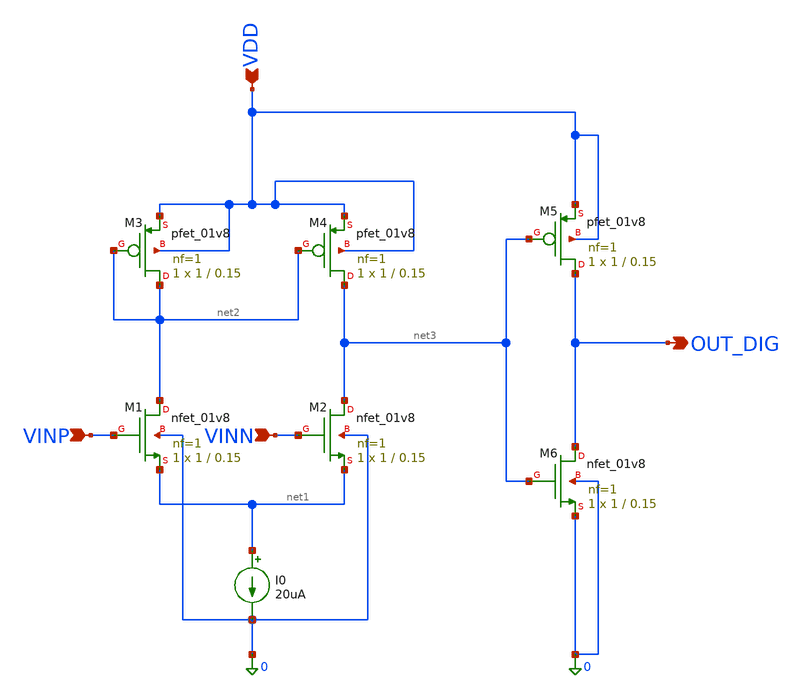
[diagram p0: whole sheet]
** sch_path: comparator.sch
**.subckt comparator VINP VINN VDD OUT_DIG
*.ipin VINP
*.ipin VINN
*.ipin VDD
*.opin OUT_DIG
I0 net1 0 20uA
XM1 net2 VINP net1 0 sky130_fd_pr__nfet_01v8 L=0.15 W=1 nf=1 ad='int((1 + 1)/2) * 1 / 1 * 0.29' as='int((1 + 2)/2) * 1 / 1 * 0.29'
+ pd='2*int((1 + 1)/2) * (1 / 1 + 0.29)' ps='2*int((1 + 2)/2) * (1 / 1 + 0.29)' nrd='0.29 / 1 ' nrs='0.29 / 1 '
+ sa=0 sb=0 sd=0 mult=1 m=1
XM2 net3 VINN net1 0 sky130_fd_pr__nfet_01v8 L=0.15 W=1 nf=1 ad='int((1 + 1)/2) * 1 / 1 * 0.29' as='int((1 + 2)/2) * 1 / 1 * 0.29'
+ pd='2*int((1 + 1)/2) * (1 / 1 + 0.29)' ps='2*int((1 + 2)/2) * (1 / 1 + 0.29)' nrd='0.29 / 1 ' nrs='0.29 / 1 '
+ sa=0 sb=0 sd=0 mult=1 m=1
XM6 OUT_DIG net3 0 0 sky130_fd_pr__nfet_01v8 L=0.15 W=1 nf=1 ad='int((1 + 1)/2) * 1 / 1 * 0.29' as='int((1 + 2)/2) * 1 / 1 * 0.29'
+ pd='2*int((1 + 1)/2) * (1 / 1 + 0.29)' ps='2*int((1 + 2)/2) * (1 / 1 + 0.29)' nrd='0.29 / 1 ' nrs='0.29 / 1 '
+ sa=0 sb=0 sd=0 mult=1 m=1
XM3 net2 net2 VDD VDD sky130_fd_pr__pfet_01v8 L=0.15 W=1 nf=1 ad='int((1 + 1)/2) * 1 / 1 * 0.29' as='int((1 + 2)/2) * 1 / 1 * 0.29'
+ pd='2*int((1 + 1)/2) * (1 / 1 + 0.29)' ps='2*int((1 + 2)/2) * (1 / 1 + 0.29)' nrd='0.29 / 1 ' nrs='0.29 / 1 '
+ sa=0 sb=0 sd=0 mult=1 m=1
XM4 net3 net2 VDD VDD sky130_fd_pr__pfet_01v8 L=0.15 W=1 nf=1 ad='int((1 + 1)/2) * 1 / 1 * 0.29' as='int((1 + 2)/2) * 1 / 1 * 0.29'
+ pd='2*int((1 + 1)/2) * (1 / 1 + 0.29)' ps='2*int((1 + 2)/2) * (1 / 1 + 0.29)' nrd='0.29 / 1 ' nrs='0.29 / 1 '
+ sa=0 sb=0 sd=0 mult=1 m=1
XM5 OUT_DIG net3 VDD VDD sky130_fd_pr__pfet_01v8 L=0.15 W=1 nf=1 ad='int((1 + 1)/2) * 1 / 1 * 0.29' as='int((1 + 2)/2) * 1 / 1 * 0.29'
+ pd='2*int((1 + 1)/2) * (1 / 1 + 0.29)' ps='2*int((1 + 2)/2) * (1 / 1 + 0.29)' nrd='0.29 / 1 ' nrs='0.29 / 1 '
+ sa=0 sb=0 sd=0 mult=1 m=1
**.ends
.end
